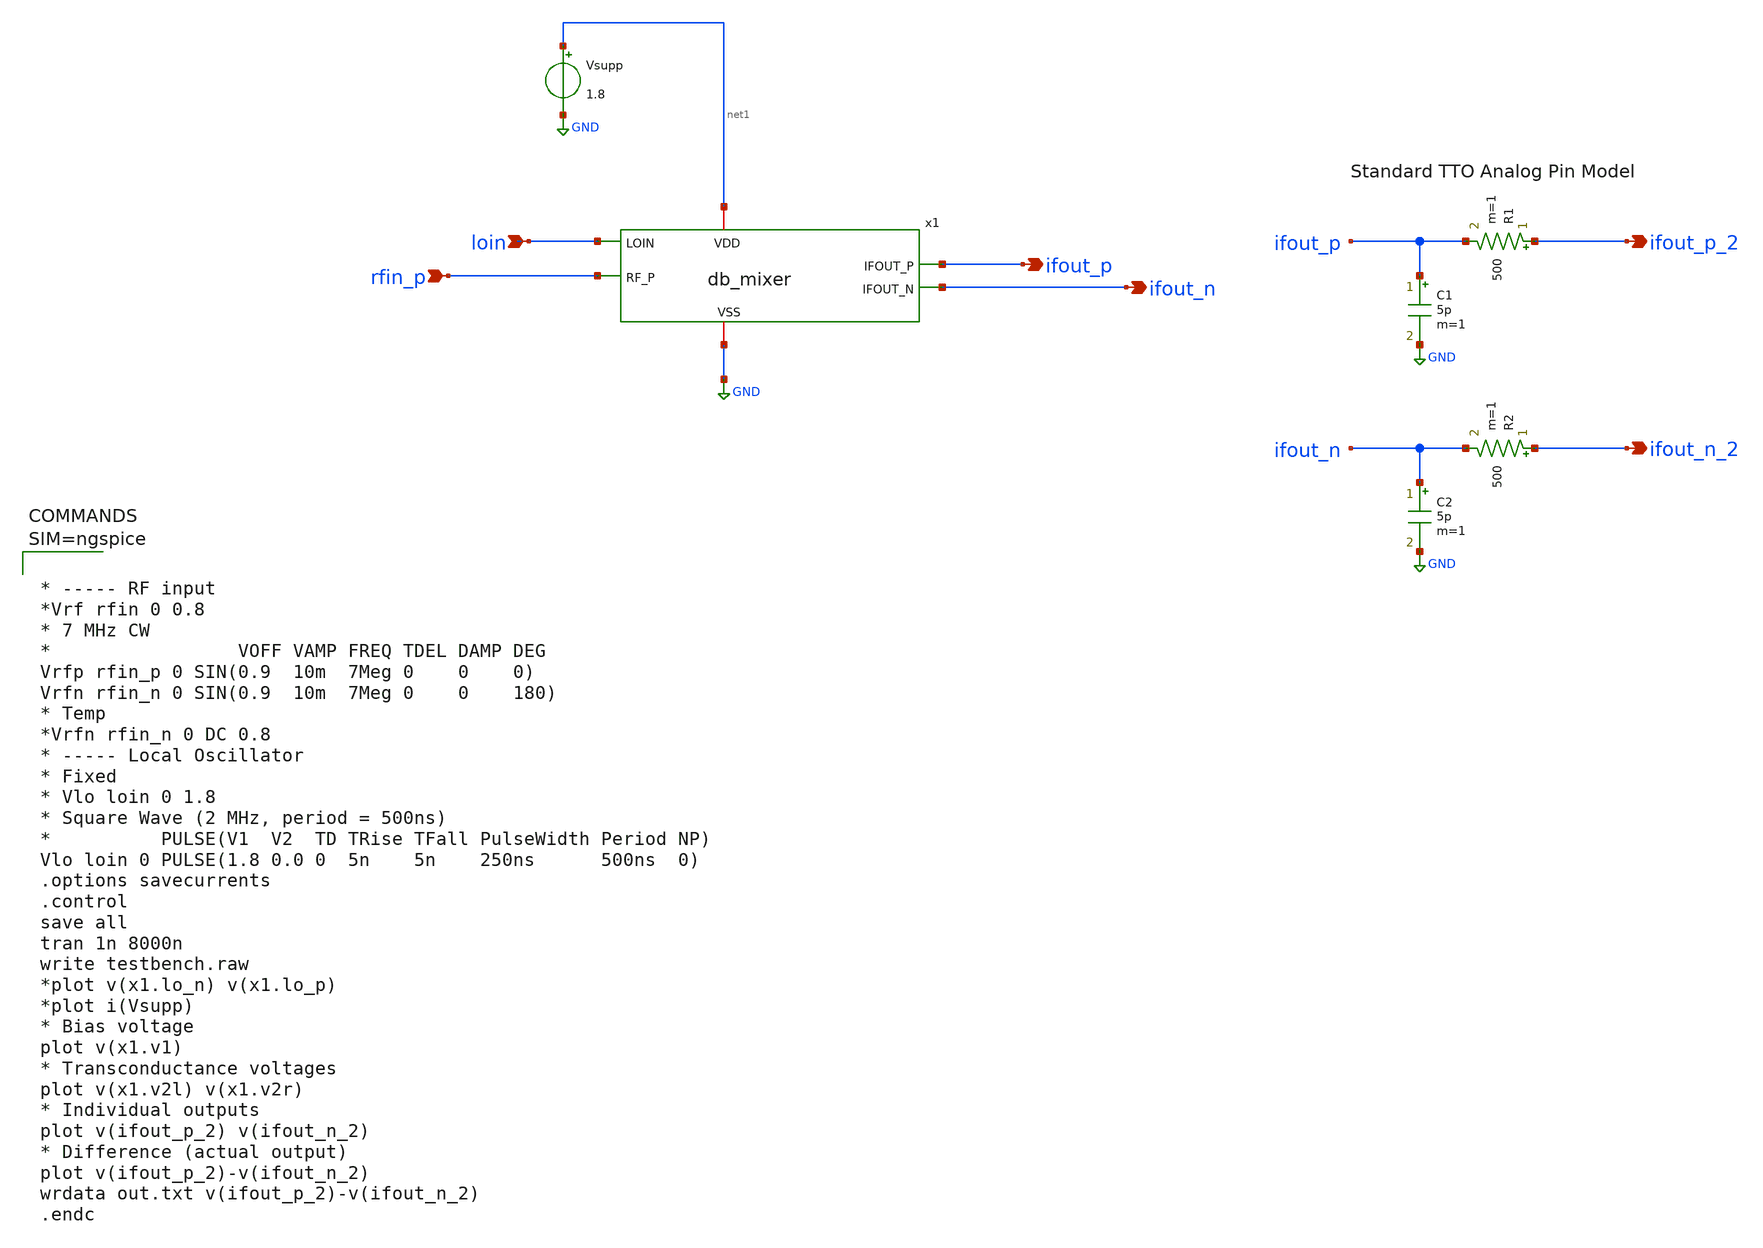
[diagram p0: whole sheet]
** sch_path: xschem/testbench_db2.sch
**.subckt testbench_db2 loin rfin_p ifout_p ifout_n ifout_p_2 ifout_n_2
*.ipin loin
*.ipin rfin_p
*.opin ifout_p
*.opin ifout_n
*.opin ifout_p_2
*.opin ifout_n_2
C1 ifout_p GND 5p m=1
R1 ifout_p_2 ifout_p 500 m=1
C2 ifout_n GND 5p m=1
R2 ifout_n_2 ifout_n 500 m=1
Vsupp net1 GND 1.8
x1 net1 GND loin ifout_n ifout_p rfin_p db_mixer
**** begin user architecture code

** opencircuitdesign pdks install
.lib $::SKYWATER_MODELS/sky130.lib.spice tt
.include $::SKYWATER_STDCELLS/sky130_fd_sc_hd.spice





* ----- RF input
*Vrf rfin 0 0.8
* 7 MHz CW
*                 VOFF VAMP FREQ TDEL DAMP DEG
Vrfp rfin_p 0 SIN(0.9  10m  7Meg 0    0    0)
Vrfn rfin_n 0 SIN(0.9  10m  7Meg 0    0    180)
* Temp
*Vrfn rfin_n 0 DC 0.8
* ----- Local Oscillator
* Fixed
* Vlo loin 0 1.8
* Square Wave (2 MHz, period = 500ns)
*          PULSE(V1  V2  TD TRise TFall PulseWidth Period NP)
Vlo loin 0 PULSE(1.8 0.0 0  5n    5n    250ns      500ns  0)
.options savecurrents
.control
save all
tran 1n 8000n
write testbench.raw
*plot v(x1.lo_n) v(x1.lo_p)
*plot i(Vsupp)
* Bias voltage
plot v(x1.v1)
* Transconductance voltages
plot v(x1.v2l) v(x1.v2r)
* Individual outputs
plot v(ifout_p_2) v(ifout_n_2)
* Difference (actual output)
plot v(ifout_p_2)-v(ifout_n_2)
wrdata out.txt v(ifout_p_2)-v(ifout_n_2)
.endc



**** end user architecture code
**.ends

* expanding   symbol:  db_mixer.sym # of pins=6
** sym_path: xschem/db_mixer.sym
** sch_path: xschem/db_mixer.sch
.subckt db_mixer VDD VSS LOIN IFOUT_N IFOUT_P RF_P
*.iopin VDD
*.iopin VSS
*.ipin LOIN
*.opin IFOUT_P
*.opin IFOUT_N
*.ipin RF_P
XM5 BIAS0 BIAS0 VSS VSS sky130_fd_pr__nfet_01v8 L=2 W=20 nf=4 ad='int((nf+1)/2) * W/nf * 0.29' as='int((nf+2)/2) * W/nf * 0.29'
+ pd='2*int((nf+1)/2) * (W/nf + 0.29)' ps='2*int((nf+2)/2) * (W/nf + 0.29)' nrd='0.29 / W' nrs='0.29 / W'
+ sa=0 sb=0 sd=0 mult=1 m=1
XM6 V1 BIAS0 VSS VSS sky130_fd_pr__nfet_01v8 L=2 W=40 nf=4 ad='int((nf+1)/2) * W/nf * 0.29' as='int((nf+2)/2) * W/nf * 0.29'
+ pd='2*int((nf+1)/2) * (W/nf + 0.29)' ps='2*int((nf+2)/2) * (W/nf + 0.29)' nrd='0.29 / W' nrs='0.29 / W'
+ sa=0 sb=0 sd=0 mult=1 m=1
XR3 BIAS0 VDD VSS sky130_fd_pr__res_high_po_0p35 L=20 mult=1 m=1
x1 LOIN VSS VSS VDD VDD LO_N sky130_fd_sc_hd__inv_1
x2 LO_N VSS VSS VDD VDD LO_P sky130_fd_sc_hd__inv_1
XM1 V2L RF_P V1 VSS sky130_fd_pr__nfet_01v8 L=2 W=10 nf=1 ad='int((nf+1)/2) * W/nf * 0.29' as='int((nf+2)/2) * W/nf * 0.29'
+ pd='2*int((nf+1)/2) * (W/nf + 0.29)' ps='2*int((nf+2)/2) * (W/nf + 0.29)' nrd='0.29 / W' nrs='0.29 / W'
+ sa=0 sb=0 sd=0 mult=1 m=1
XM2 V2R RF_N V1 VSS sky130_fd_pr__nfet_01v8 L=2 W=10 nf=1 ad='int((nf+1)/2) * W/nf * 0.29' as='int((nf+2)/2) * W/nf * 0.29'
+ pd='2*int((nf+1)/2) * (W/nf + 0.29)' ps='2*int((nf+2)/2) * (W/nf + 0.29)' nrd='0.29 / W' nrs='0.29 / W'
+ sa=0 sb=0 sd=0 mult=1 m=1
XM3 IFOUT_P LO_N V2L VSS sky130_fd_pr__nfet_01v8 L=2 W=10 nf=1 ad='int((nf+1)/2) * W/nf * 0.29' as='int((nf+2)/2) * W/nf * 0.29'
+ pd='2*int((nf+1)/2) * (W/nf + 0.29)' ps='2*int((nf+2)/2) * (W/nf + 0.29)' nrd='0.29 / W' nrs='0.29 / W'
+ sa=0 sb=0 sd=0 mult=1 m=1
XM4 IFOUT_N LO_P V2L VSS sky130_fd_pr__nfet_01v8 L=2 W=10 nf=1 ad='int((nf+1)/2) * W/nf * 0.29' as='int((nf+2)/2) * W/nf * 0.29'
+ pd='2*int((nf+1)/2) * (W/nf + 0.29)' ps='2*int((nf+2)/2) * (W/nf + 0.29)' nrd='0.29 / W' nrs='0.29 / W'
+ sa=0 sb=0 sd=0 mult=1 m=1
XM7 IFOUT_P LO_P V2R VSS sky130_fd_pr__nfet_01v8 L=2 W=10 nf=1 ad='int((nf+1)/2) * W/nf * 0.29' as='int((nf+2)/2) * W/nf * 0.29'
+ pd='2*int((nf+1)/2) * (W/nf + 0.29)' ps='2*int((nf+2)/2) * (W/nf + 0.29)' nrd='0.29 / W' nrs='0.29 / W'
+ sa=0 sb=0 sd=0 mult=1 m=1
XM8 IFOUT_N LO_N V2R VSS sky130_fd_pr__nfet_01v8 L=2 W=10 nf=1 ad='int((nf+1)/2) * W/nf * 0.29' as='int((nf+2)/2) * W/nf * 0.29'
+ pd='2*int((nf+1)/2) * (W/nf + 0.29)' ps='2*int((nf+2)/2) * (W/nf + 0.29)' nrd='0.29 / W' nrs='0.29 / W'
+ sa=0 sb=0 sd=0 mult=1 m=1
XR1 IFOUT_P VDD VSS sky130_fd_pr__res_high_po_0p69 L=0.69 mult=1 m=1
XR2 IFOUT_N VDD VSS sky130_fd_pr__res_high_po_0p69 L=0.69 mult=1 m=1
XR4 RF_N VDD VSS sky130_fd_pr__res_high_po_0p35 L=10 mult=1 m=1
XR5 VSS RF_N VSS sky130_fd_pr__res_high_po_0p35 L=10 mult=1 m=1
.ends

.GLOBAL GND
.end
